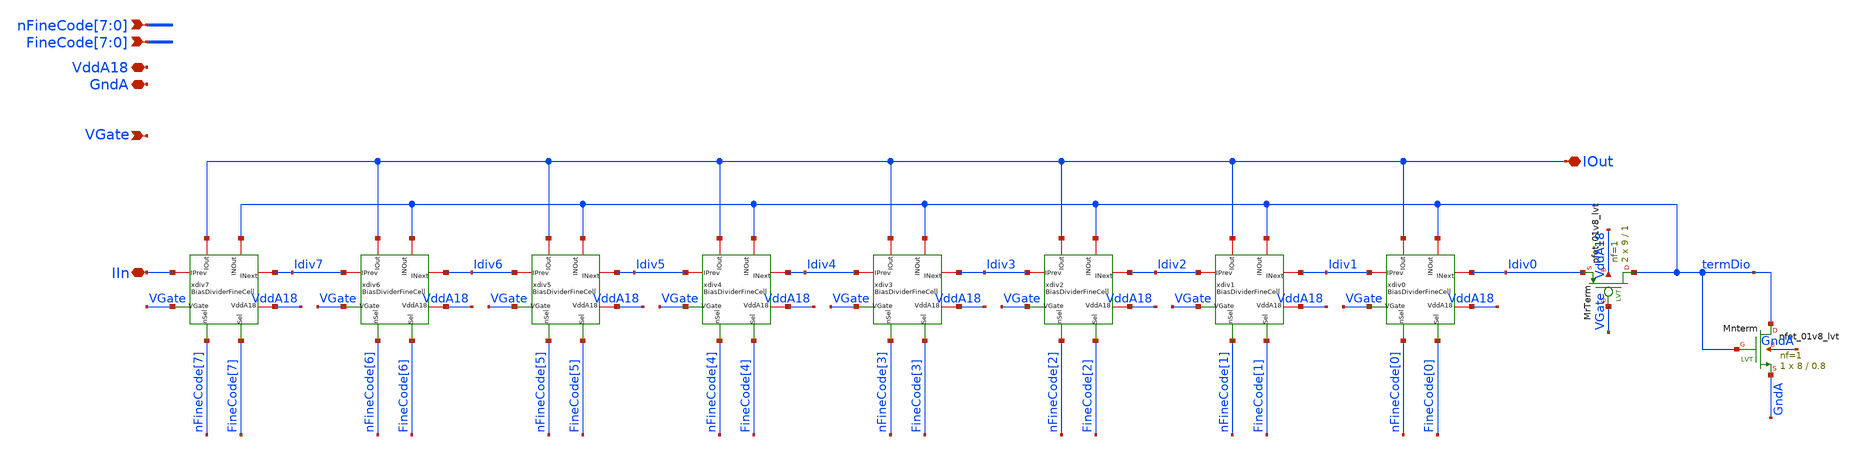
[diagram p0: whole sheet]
** sch_path: analog/klayout/production/final_merge_20260923/testbenches/cace/analog/xschem/BiasDividerFine.sch
**.subckt BiasDividerFine VddA18 GndA IOut
*+ FineCode[7],FineCode[6],FineCode[5],FineCode[4],FineCode[3],FineCode[2],FineCode[1],FineCode[0] VGate IIn
*+ nFineCode[7],nFineCode[6],nFineCode[5],nFineCode[4],nFineCode[3],nFineCode[2],nFineCode[1],nFineCode[0]
*.iopin VddA18
*.iopin GndA
*.iopin IOut
*.ipin
*+ FineCode[7],FineCode[6],FineCode[5],FineCode[4],FineCode[3],FineCode[2],FineCode[1],FineCode[0]
*.ipin VGate
*.iopin IIn
*.ipin
*+ nFineCode[7],nFineCode[6],nFineCode[5],nFineCode[4],nFineCode[3],nFineCode[2],nFineCode[1],nFineCode[0]
xdiv0 Idiv1 Idiv0 VGate IOut VddA18 termDio nFineCode[0] FineCode[0] BiasDividerFineCell
xdiv1 Idiv2 Idiv1 VGate IOut VddA18 termDio nFineCode[1] FineCode[1] BiasDividerFineCell
xdiv2 Idiv3 Idiv2 VGate IOut VddA18 termDio nFineCode[2] FineCode[2] BiasDividerFineCell
xdiv3 Idiv4 Idiv3 VGate IOut VddA18 termDio nFineCode[3] FineCode[3] BiasDividerFineCell
xdiv4 Idiv5 Idiv4 VGate IOut VddA18 termDio nFineCode[4] FineCode[4] BiasDividerFineCell
xdiv5 Idiv6 Idiv5 VGate IOut VddA18 termDio nFineCode[5] FineCode[5] BiasDividerFineCell
xdiv6 Idiv7 Idiv6 VGate IOut VddA18 termDio nFineCode[6] FineCode[6] BiasDividerFineCell
xdiv7 IIn Idiv7 VGate IOut VddA18 termDio nFineCode[7] FineCode[7] BiasDividerFineCell
XMrTerm termDio VGate Idiv0 VddA18 sky130_fd_pr__pfet_01v8_lvt L=1 W=9 nf=1 ad='int((1 + 1)/2) * 9 / 1 * 0.29'
+ as='int((1 + 2)/2) * 9 / 1 * 0.29' pd='2*int((1 + 1)/2) * (9 / 1 + 0.29)' ps='2*int((1 + 2)/2) * (9 / 1 + 0.29)'
+ nrd='0.29 / 9 ' nrs='0.29 / 9 ' sa=0 sb=0 sd=0 mult=2 m=2
XMnterm termDio termDio GndA GndA sky130_fd_pr__nfet_01v8_lvt L=0.8 W=8 nf=1 ad='int((1 + 1)/2) * 8 / 1 * 0.29'
+ as='int((1 + 2)/2) * 8 / 1 * 0.29' pd='2*int((1 + 1)/2) * (8 / 1 + 0.29)' ps='2*int((1 + 2)/2) * (8 / 1 + 0.29)'
+ nrd='0.29 / 8 ' nrs='0.29 / 8 ' sa=0 sb=0 sd=0 mult=1 m=1
**.ends

* expanding   symbol:  BiasDividerFineCell.sym # of pins=8
** sym_path: analog/xschem/BiasDividerFineCell.sym
** sch_path: analog/xschem/BiasDividerFineCell.sch
.subckt BiasDividerFineCell IPrev INext VGate IOut VddA18 INOut nSel Sel
*.iopin INext
*.iopin IOut
*.iopin IPrev
*.ipin VGate
*.iopin VddA18
*.ipin nSel
*.ipin Sel
*.iopin INOut
XMr INext VGate IPrev VddA18 sky130_fd_pr__pfet_01v8 L=1 W=9 nf=1 ad='int((1 + 1)/2) * 9 / 1 * 0.29'
+ as='int((1 + 2)/2) * 9 / 1 * 0.29' pd='2*int((1 + 1)/2) * (9 / 1 + 0.29)' ps='2*int((1 + 2)/2) * (9 / 1 + 0.29)'
+ nrd='0.29 / 9 ' nrs='0.29 / 9 ' sa=0 sb=0 sd=0 mult=2 m=2
XM2ru net1 VGate IPrev VddA18 sky130_fd_pr__pfet_01v8 L=1 W=9 nf=1 ad='int((1 + 1)/2) * 9 / 1 * 0.29'
+ as='int((1 + 2)/2) * 9 / 1 * 0.29' pd='2*int((1 + 1)/2) * (9 / 1 + 0.29)' ps='2*int((1 + 2)/2) * (9 / 1 + 0.29)'
+ nrd='0.29 / 9 ' nrs='0.29 / 9 ' sa=0 sb=0 sd=0 mult=2 m=2
XM2rl net2 VGate net1 VddA18 sky130_fd_pr__pfet_01v8 L=1 W=9 nf=1 ad='int((1 + 1)/2) * 9 / 1 * 0.29'
+ as='int((1 + 2)/2) * 9 / 1 * 0.29' pd='2*int((1 + 1)/2) * (9 / 1 + 0.29)' ps='2*int((1 + 2)/2) * (9 / 1 + 0.29)'
+ nrd='0.29 / 9 ' nrs='0.29 / 9 ' sa=0 sb=0 sd=0 mult=2 m=2
XMswNOut INOut Sel net2 VddA18 sky130_fd_pr__pfet_01v8 L=0.5 W=2 nf=1 ad='int((1 + 1)/2) * 2 / 1 * 0.29'
+ as='int((1 + 2)/2) * 2 / 1 * 0.29' pd='2*int((1 + 1)/2) * (2 / 1 + 0.29)' ps='2*int((1 + 2)/2) * (2 / 1 + 0.29)'
+ nrd='0.29 / 2 ' nrs='0.29 / 2 ' sa=0 sb=0 sd=0 mult=1 m=1
XMswOut IOut nSel net2 VddA18 sky130_fd_pr__pfet_01v8 L=0.5 W=2 nf=1 ad='int((1 + 1)/2) * 2 / 1 * 0.29'
+ as='int((1 + 2)/2) * 2 / 1 * 0.29' pd='2*int((1 + 1)/2) * (2 / 1 + 0.29)' ps='2*int((1 + 2)/2) * (2 / 1 + 0.29)'
+ nrd='0.29 / 2 ' nrs='0.29 / 2 ' sa=0 sb=0 sd=0 mult=1 m=1
.ends

.end
